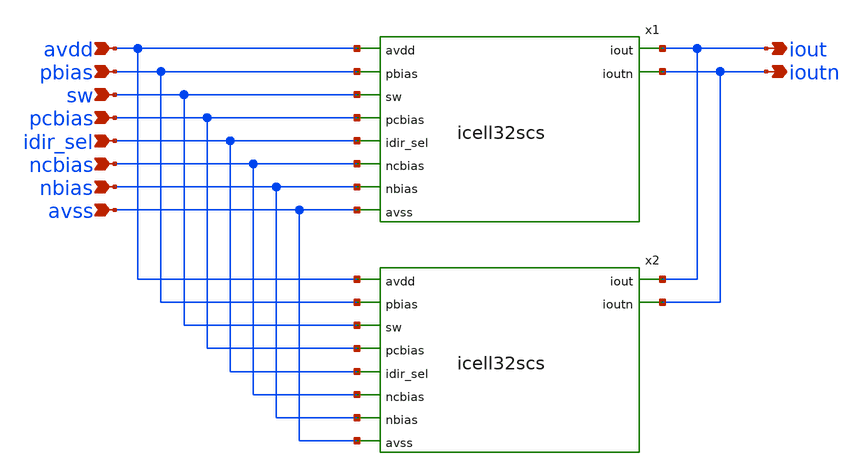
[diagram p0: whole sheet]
** sch_path: xschem/icell64scs.sch
**.subckt icell64scs avdd pbias sw pcbias idir_sel ncbias nbias avss iout ioutn
*.ipin avdd
*.ipin pbias
*.ipin sw
*.ipin pcbias
*.ipin idir_sel
*.ipin ncbias
*.ipin nbias
*.ipin avss
*.opin iout
*.opin ioutn
x1 iout avdd pbias ioutn sw pcbias idir_sel ncbias nbias avss icell32scs
x2 iout avdd pbias ioutn sw pcbias idir_sel ncbias nbias avss icell32scs
**.ends
.end
